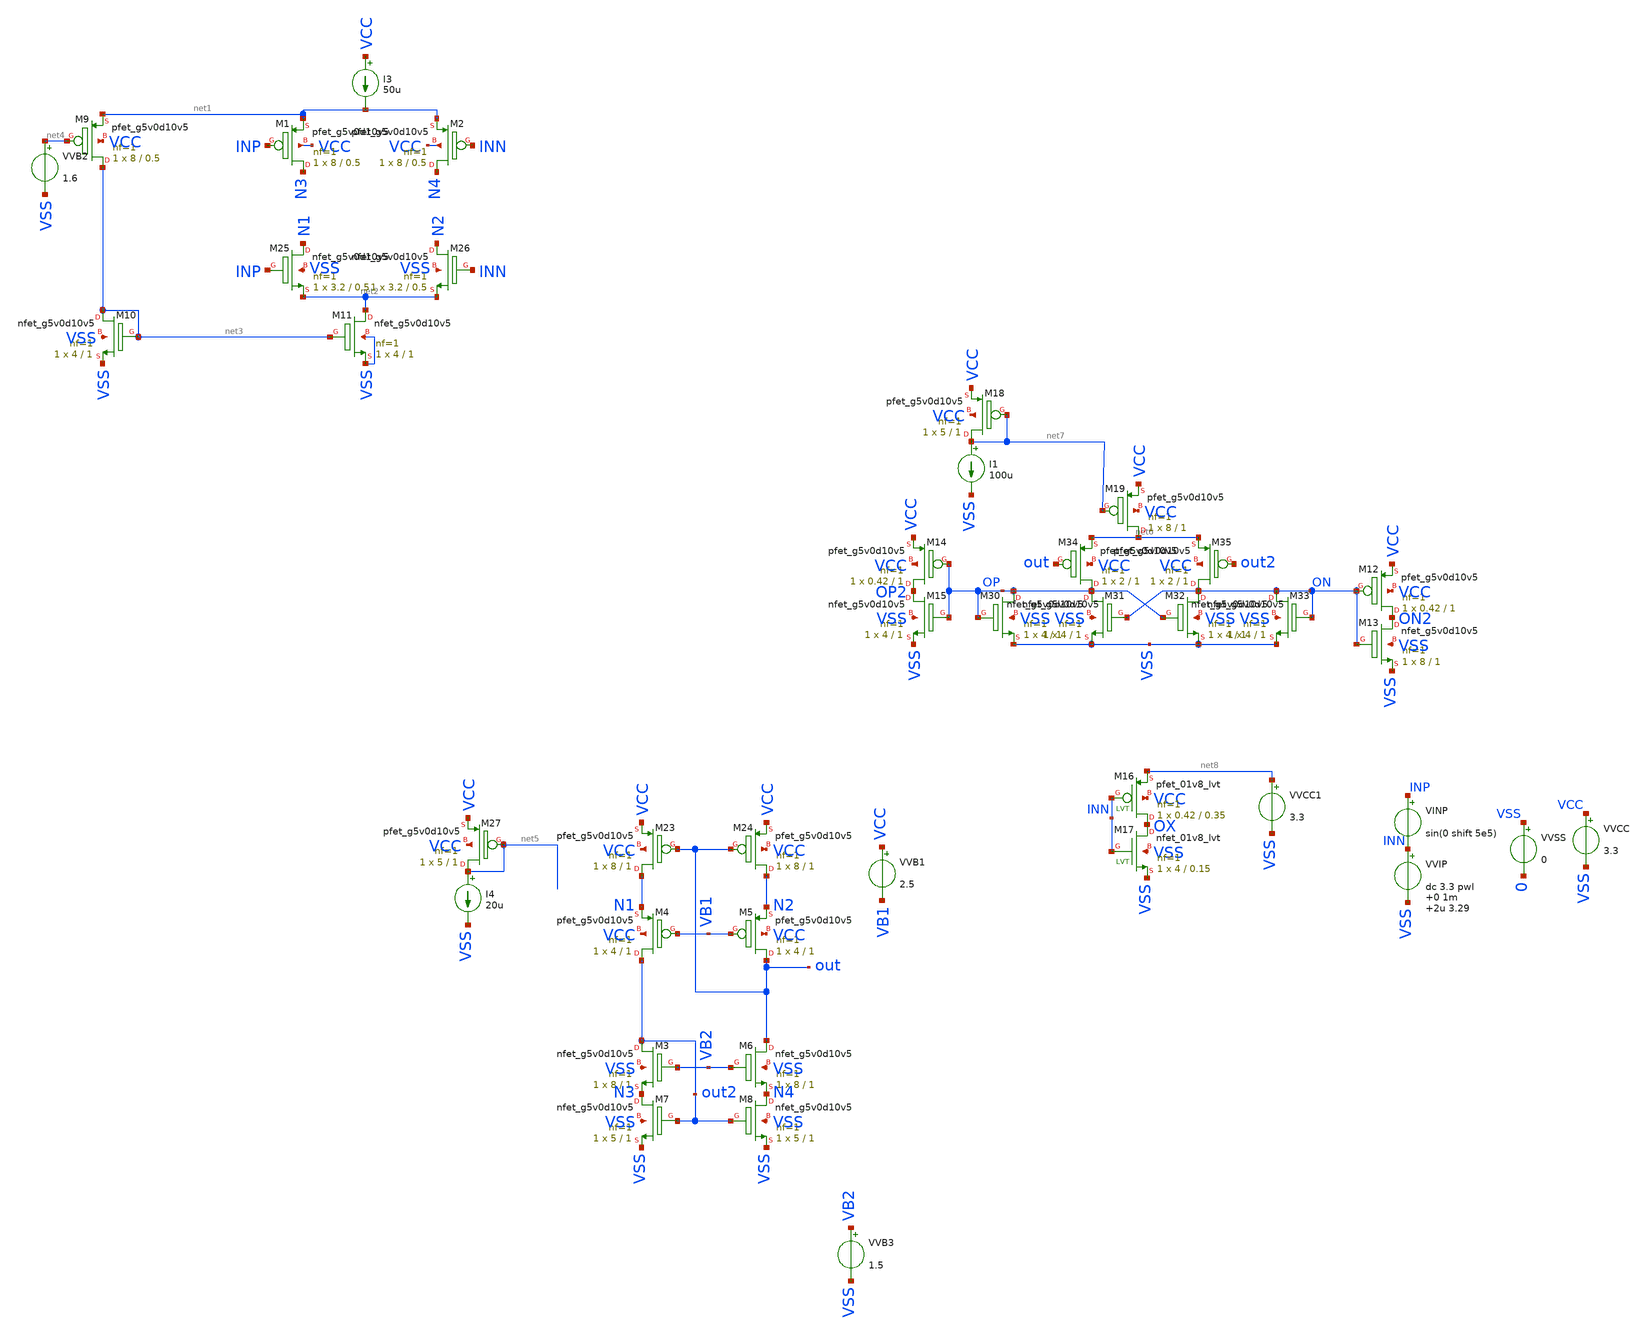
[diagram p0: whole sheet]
** sch_path: folded_cascode/folded_cascode_2.sch
.lib $::SKYWATER_MODELS/sky130.lib.spice.ss.red ss
.include $::SKYWATER_STDCELLS/sky130_fd_sc_hd.spice

**.subckt folded_cascode_2
VINP INP INN sin(0 shift 5e5)
VVSS VSS 0 0
VVCC VCC VSS 3.3
VVIP INN VSS dc 3.3 pwl 0 1m 2u 3.29

XM25 N1 INP net2 VSS sky130_fd_pr__nfet_g5v0d10v5 L=0.5 W=3.2 nf=1 ad='int((nf+1)/2) * W/nf * 0.29' as='int((nf+2)/2) * W/nf * 0.29'
+ pd='2*int((nf+1)/2) * (W/nf + 0.29)' ps='2*int((nf+2)/2) * (W/nf + 0.29)' nrd='0.29 / W' nrs='0.29 / W'
+ sa=0 sb=0 sd=0 mult=1 m=1
XM26 N2 INN net2 VSS sky130_fd_pr__nfet_g5v0d10v5 L=0.5 W=3.2 nf=1 ad='int((nf+1)/2) * W/nf * 0.29' as='int((nf+2)/2) * W/nf * 0.29'
+ pd='2*int((nf+1)/2) * (W/nf + 0.29)' ps='2*int((nf+2)/2) * (W/nf + 0.29)' nrd='0.29 / W' nrs='0.29 / W'
+ sa=0 sb=0 sd=0 mult=1 m=1
XM1 N3 INP net1 VCC sky130_fd_pr__pfet_g5v0d10v5 L=0.5 W=8 nf=1 ad='int((nf+1)/2) * W/nf * 0.29' as='int((nf+2)/2) * W/nf * 0.29'
+ pd='2*int((nf+1)/2) * (W/nf + 0.29)' ps='2*int((nf+2)/2) * (W/nf + 0.29)' nrd='0.29 / W' nrs='0.29 / W'
+ sa=0 sb=0 sd=0 mult=1 m=1
XM2 N4 INN net1 VCC sky130_fd_pr__pfet_g5v0d10v5 L=0.5 W=8 nf=1 ad='int((nf+1)/2) * W/nf * 0.29' as='int((nf+2)/2) * W/nf * 0.29'
+ pd='2*int((nf+1)/2) * (W/nf + 0.29)' ps='2*int((nf+2)/2) * (W/nf + 0.29)' nrd='0.29 / W' nrs='0.29 / W'
+ sa=0 sb=0 sd=0 mult=1 m=1
XM9 net3 net4 net1 VCC sky130_fd_pr__pfet_g5v0d10v5 L=0.5 W=8 nf=1 ad='int((nf+1)/2) * W/nf * 0.29' as='int((nf+2)/2) * W/nf * 0.29'
+ pd='2*int((nf+1)/2) * (W/nf + 0.29)' ps='2*int((nf+2)/2) * (W/nf + 0.29)' nrd='0.29 / W' nrs='0.29 / W'
+ sa=0 sb=0 sd=0 mult=1 m=1
XM10 net3 net3 VSS VSS sky130_fd_pr__nfet_g5v0d10v5 L=1 W=4 nf=1 ad='int((nf+1)/2) * W/nf * 0.29' as='int((nf+2)/2) * W/nf * 0.29'
+ pd='2*int((nf+1)/2) * (W/nf + 0.29)' ps='2*int((nf+2)/2) * (W/nf + 0.29)' nrd='0.29 / W' nrs='0.29 / W'
+ sa=0 sb=0 sd=0 mult=1 m=1
VVB2 net4 VSS 1.6
XM11 net2 net3 VSS VSS sky130_fd_pr__nfet_g5v0d10v5 L=1 W=4 nf=1 ad='int((nf+1)/2) * W/nf * 0.29' as='int((nf+2)/2) * W/nf * 0.29'
+ pd='2*int((nf+1)/2) * (W/nf + 0.29)' ps='2*int((nf+2)/2) * (W/nf + 0.29)' nrd='0.29 / W' nrs='0.29 / W'
+ sa=0 sb=0 sd=0 mult=1 m=1
XM4 out2 VB1 N1 VCC sky130_fd_pr__pfet_g5v0d10v5 L=1 W=4 nf=1 ad='int((nf+1)/2) * W/nf * 0.29' as='int((nf+2)/2) * W/nf * 0.29'
+ pd='2*int((nf+1)/2) * (W/nf + 0.29)' ps='2*int((nf+2)/2) * (W/nf + 0.29)' nrd='0.29 / W' nrs='0.29 / W'
+ sa=0 sb=0 sd=0 mult=1 m=1
XM5 out VB1 N2 VCC sky130_fd_pr__pfet_g5v0d10v5 L=1 W=4 nf=1 ad='int((nf+1)/2) * W/nf * 0.29' as='int((nf+2)/2) * W/nf * 0.29'
+ pd='2*int((nf+1)/2) * (W/nf + 0.29)' ps='2*int((nf+2)/2) * (W/nf + 0.29)' nrd='0.29 / W' nrs='0.29 / W'
+ sa=0 sb=0 sd=0 mult=1 m=1
I3 VCC net1 50u
XM3 out2 VB2 N3 VSS sky130_fd_pr__nfet_g5v0d10v5 L=1 W=8 nf=1 ad='int((nf+1)/2) * W/nf * 0.29' as='int((nf+2)/2) * W/nf * 0.29'
+ pd='2*int((nf+1)/2) * (W/nf + 0.29)' ps='2*int((nf+2)/2) * (W/nf + 0.29)' nrd='0.29 / W' nrs='0.29 / W'
+ sa=0 sb=0 sd=0 mult=1 m=1
XM6 out VB2 N4 VSS sky130_fd_pr__nfet_g5v0d10v5 L=1 W=8 nf=1 ad='int((nf+1)/2) * W/nf * 0.29' as='int((nf+2)/2) * W/nf * 0.29'
+ pd='2*int((nf+1)/2) * (W/nf + 0.29)' ps='2*int((nf+2)/2) * (W/nf + 0.29)' nrd='0.29 / W' nrs='0.29 / W'
+ sa=0 sb=0 sd=0 mult=1 m=1
XM7 N3 out2 VSS VSS sky130_fd_pr__nfet_g5v0d10v5 L=1 W=5 nf=1 ad='int((nf+1)/2) * W/nf * 0.29' as='int((nf+2)/2) * W/nf * 0.29'
+ pd='2*int((nf+1)/2) * (W/nf + 0.29)' ps='2*int((nf+2)/2) * (W/nf + 0.29)' nrd='0.29 / W' nrs='0.29 / W'
+ sa=0 sb=0 sd=0 mult=1 m=1
XM8 N4 out2 VSS VSS sky130_fd_pr__nfet_g5v0d10v5 L=1 W=5 nf=1 ad='int((nf+1)/2) * W/nf * 0.29' as='int((nf+2)/2) * W/nf * 0.29'
+ pd='2*int((nf+1)/2) * (W/nf + 0.29)' ps='2*int((nf+2)/2) * (W/nf + 0.29)' nrd='0.29 / W' nrs='0.29 / W'
+ sa=0 sb=0 sd=0 mult=1 m=1
VVB1 VCC VB1 2.5
VVB3 VB2 VSS 1.5
XM23 N1 out VCC VCC sky130_fd_pr__pfet_g5v0d10v5 L=1 W=8 nf=1 ad='int((nf+1)/2) * W/nf * 0.29' as='int((nf+2)/2) * W/nf * 0.29'
+ pd='2*int((nf+1)/2) * (W/nf + 0.29)' ps='2*int((nf+2)/2) * (W/nf + 0.29)' nrd='0.29 / W' nrs='0.29 / W'
+ sa=0 sb=0 sd=0 mult=1 m=1
XM24 N2 out VCC VCC sky130_fd_pr__pfet_g5v0d10v5 L=1 W=8 nf=1 ad='int((nf+1)/2) * W/nf * 0.29' as='int((nf+2)/2) * W/nf * 0.29'
+ pd='2*int((nf+1)/2) * (W/nf + 0.29)' ps='2*int((nf+2)/2) * (W/nf + 0.29)' nrd='0.29 / W' nrs='0.29 / W'
+ sa=0 sb=0 sd=0 mult=1 m=1
XM27 net5 net5 VCC VCC sky130_fd_pr__pfet_g5v0d10v5 L=1 W=5 nf=1 ad='int((nf+1)/2) * W/nf * 0.29' as='int((nf+2)/2) * W/nf * 0.29'
+ pd='2*int((nf+1)/2) * (W/nf + 0.29)' ps='2*int((nf+2)/2) * (W/nf + 0.29)' nrd='0.29 / W' nrs='0.29 / W'
+ sa=0 sb=0 sd=0 mult=1 m=1
I4 net5 VSS 20u
XM30 OP OP VSS VSS sky130_fd_pr__nfet_g5v0d10v5 L=1 W=4 nf=1 ad='int((nf+1)/2) * W/nf * 0.29' as='int((nf+2)/2) * W/nf * 0.29'
+ pd='2*int((nf+1)/2) * (W/nf + 0.29)' ps='2*int((nf+2)/2) * (W/nf + 0.29)' nrd='0.29 / W' nrs='0.29 / W'
+ sa=0 sb=0 sd=0 mult=1 m=1
XM31 OP ON VSS VSS sky130_fd_pr__nfet_g5v0d10v5 L=1 W=4 nf=1 ad='int((nf+1)/2) * W/nf * 0.29' as='int((nf+2)/2) * W/nf * 0.29'
+ pd='2*int((nf+1)/2) * (W/nf + 0.29)' ps='2*int((nf+2)/2) * (W/nf + 0.29)' nrd='0.29 / W' nrs='0.29 / W'
+ sa=0 sb=0 sd=0 mult=1 m=1
XM32 ON OP VSS VSS sky130_fd_pr__nfet_g5v0d10v5 L=1 W=4 nf=1 ad='int((nf+1)/2) * W/nf * 0.29' as='int((nf+2)/2) * W/nf * 0.29'
+ pd='2*int((nf+1)/2) * (W/nf + 0.29)' ps='2*int((nf+2)/2) * (W/nf + 0.29)' nrd='0.29 / W' nrs='0.29 / W'
+ sa=0 sb=0 sd=0 mult=1 m=1
XM33 ON ON VSS VSS sky130_fd_pr__nfet_g5v0d10v5 L=1 W=4 nf=1 ad='int((nf+1)/2) * W/nf * 0.29' as='int((nf+2)/2) * W/nf * 0.29'
+ pd='2*int((nf+1)/2) * (W/nf + 0.29)' ps='2*int((nf+2)/2) * (W/nf + 0.29)' nrd='0.29 / W' nrs='0.29 / W'
+ sa=0 sb=0 sd=0 mult=1 m=1
XM34 OP out net6 VCC sky130_fd_pr__pfet_g5v0d10v5 L=1 W=2 nf=1 ad='int((nf+1)/2) * W/nf * 0.29' as='int((nf+2)/2) * W/nf * 0.29'
+ pd='2*int((nf+1)/2) * (W/nf + 0.29)' ps='2*int((nf+2)/2) * (W/nf + 0.29)' nrd='0.29 / W' nrs='0.29 / W'
+ sa=0 sb=0 sd=0 mult=1 m=1
XM35 ON out2 net6 VCC sky130_fd_pr__pfet_g5v0d10v5 L=1 W=2 nf=1 ad='int((nf+1)/2) * W/nf * 0.29' as='int((nf+2)/2) * W/nf * 0.29'
+ pd='2*int((nf+1)/2) * (W/nf + 0.29)' ps='2*int((nf+2)/2) * (W/nf + 0.29)' nrd='0.29 / W' nrs='0.29 / W'
+ sa=0 sb=0 sd=0 mult=1 m=1
XM12 ON2 ON VCC VCC sky130_fd_pr__pfet_g5v0d10v5 L=1 W=0.42 nf=1 ad='int((nf+1)/2) * W/nf * 0.29' as='int((nf+2)/2) * W/nf * 0.29'
+ pd='2*int((nf+1)/2) * (W/nf + 0.29)' ps='2*int((nf+2)/2) * (W/nf + 0.29)' nrd='0.29 / W' nrs='0.29 / W'
+ sa=0 sb=0 sd=0 mult=1 m=1
XM13 ON2 ON VSS VSS sky130_fd_pr__nfet_g5v0d10v5 L=1 W=8 nf=1 ad='int((nf+1)/2) * W/nf * 0.29' as='int((nf+2)/2) * W/nf * 0.29'
+ pd='2*int((nf+1)/2) * (W/nf + 0.29)' ps='2*int((nf+2)/2) * (W/nf + 0.29)' nrd='0.29 / W' nrs='0.29 / W'
+ sa=0 sb=0 sd=0 mult=1 m=1
XM14 OP2 OP VCC VCC sky130_fd_pr__pfet_g5v0d10v5 L=1 W=0.42 nf=1 ad='int((nf+1)/2) * W/nf * 0.29' as='int((nf+2)/2) * W/nf * 0.29'
+ pd='2*int((nf+1)/2) * (W/nf + 0.29)' ps='2*int((nf+2)/2) * (W/nf + 0.29)' nrd='0.29 / W' nrs='0.29 / W'
+ sa=0 sb=0 sd=0 mult=1 m=1
XM15 OP2 OP VSS VSS sky130_fd_pr__nfet_g5v0d10v5 L=1 W=4 nf=1 ad='int((nf+1)/2) * W/nf * 0.29' as='int((nf+2)/2) * W/nf * 0.29'
+ pd='2*int((nf+1)/2) * (W/nf + 0.29)' ps='2*int((nf+2)/2) * (W/nf + 0.29)' nrd='0.29 / W' nrs='0.29 / W'
+ sa=0 sb=0 sd=0 mult=1 m=1
XM18 net7 net7 VCC VCC sky130_fd_pr__pfet_g5v0d10v5 L=1 W=5 nf=1 ad='int((nf+1)/2) * W/nf * 0.29' as='int((nf+2)/2) * W/nf * 0.29'
+ pd='2*int((nf+1)/2) * (W/nf + 0.29)' ps='2*int((nf+2)/2) * (W/nf + 0.29)' nrd='0.29 / W' nrs='0.29 / W'
+ sa=0 sb=0 sd=0 mult=1 m=1
I1 net7 VSS 100u
XM19 net6 net7 VCC VCC sky130_fd_pr__pfet_g5v0d10v5 L=1 W=8 nf=1 ad='int((nf+1)/2) * W/nf * 0.29' as='int((nf+2)/2) * W/nf * 0.29'
+ pd='2*int((nf+1)/2) * (W/nf + 0.29)' ps='2*int((nf+2)/2) * (W/nf + 0.29)' nrd='0.29 / W' nrs='0.29 / W'
+ sa=0 sb=0 sd=0 mult=1 m=1
XM16 OX INN net8 VCC sky130_fd_pr__pfet_01v8_lvt L=0.35 W=0.42 nf=1 ad='int((nf+1)/2) * W/nf * 0.29'
+ as='int((nf+2)/2) * W/nf * 0.29' pd='2*int((nf+1)/2) * (W/nf + 0.29)' ps='2*int((nf+2)/2) * (W/nf + 0.29)'
+ nrd='0.29 / W' nrs='0.29 / W' sa=0 sb=0 sd=0 mult=1 m=1
XM17 OX INN VSS VSS sky130_fd_pr__nfet_01v8_lvt L=0.15 W=4 nf=1 ad='int((nf+1)/2) * W/nf * 0.29' as='int((nf+2)/2) * W/nf * 0.29'
+ pd='2*int((nf+1)/2) * (W/nf + 0.29)' ps='2*int((nf+2)/2) * (W/nf + 0.29)' nrd='0.29 / W' nrs='0.29 / W'
+ sa=0 sb=0 sd=0 mult=1 m=1
VVCC1 net8 VSS 3.3
**** begin user architecture code



.param ton = 30n
.param vip = .05
.param shift = 1m
.param Is = 2u
.param Iab = 2u
.option savecurrents
.save all
.save @m.xm26.msky130_fd_pr__nfet_g5v0d10v5[gm]
.save @m.xm2.msky130_fd_pr__pfet_g5v0d10v5[gm]
.tran 10n 2u
*.dc VVIP 0 3.3 0.1
**** interactive sim
.control
set color0=white
run
*set filetype=ascii
write folded_cascode_2.raw
*plot inn-inp

*plot out

quit
.endc



**** end user architecture code
**.ends
.end
